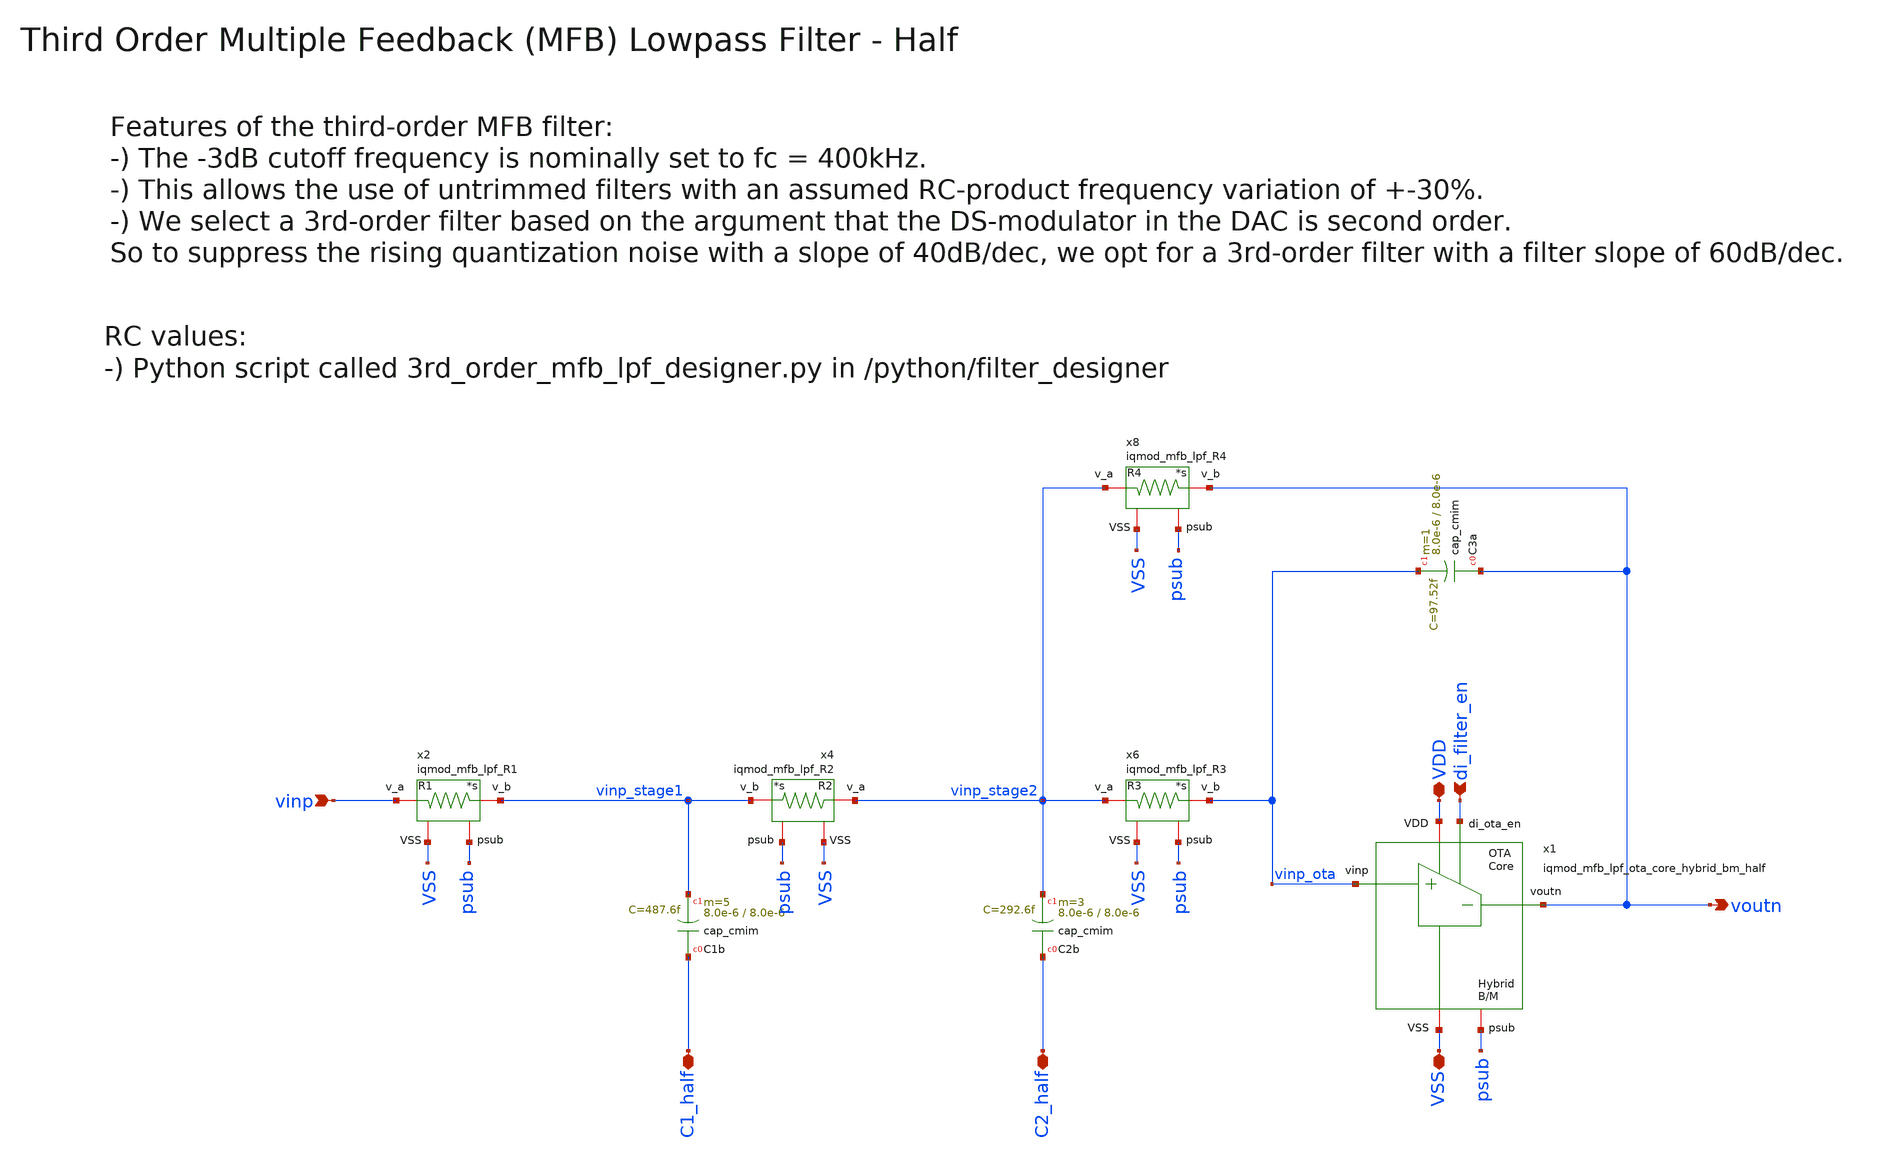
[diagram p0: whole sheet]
** sch_path: ihp130/macros/iqmod/xschem/iqmod_mfb_lpf_half.sch
**.subckt iqmod_mfb_lpf_half VDD VSS vinp voutn di_filter_en C1_half C2_half
*.iopin VDD
*.iopin VSS
*.ipin vinp
*.opin voutn
*.ipin di_filter_en
*.iopin C1_half
*.iopin C2_half
XC1b C1_half vinp_stage1 cap_cmim w=8.0e-6 l=8.0e-6 m=5 mm_ok=1
XC2b C2_half vinp_stage2 cap_cmim w=8.0e-6 l=8.0e-6 m=3 mm_ok=1
XC3a voutn vinp_ota cap_cmim w=8.0e-6 l=8.0e-6 m=1 mm_ok=1
x2 psub vinp_stage1 vinp VSS iqmod_mfb_lpf_R1
x4 vinp_stage1 vinp_stage2 psub VSS iqmod_mfb_lpf_R2
x6 vinp_ota vinp_stage2 psub VSS iqmod_mfb_lpf_R3
x8 voutn vinp_stage2 psub VSS iqmod_mfb_lpf_R4
x1 psub voutn vinp_ota VDD VSS di_filter_en iqmod_mfb_lpf_ota_core_hybrid_bm_half
**.ends
.end
